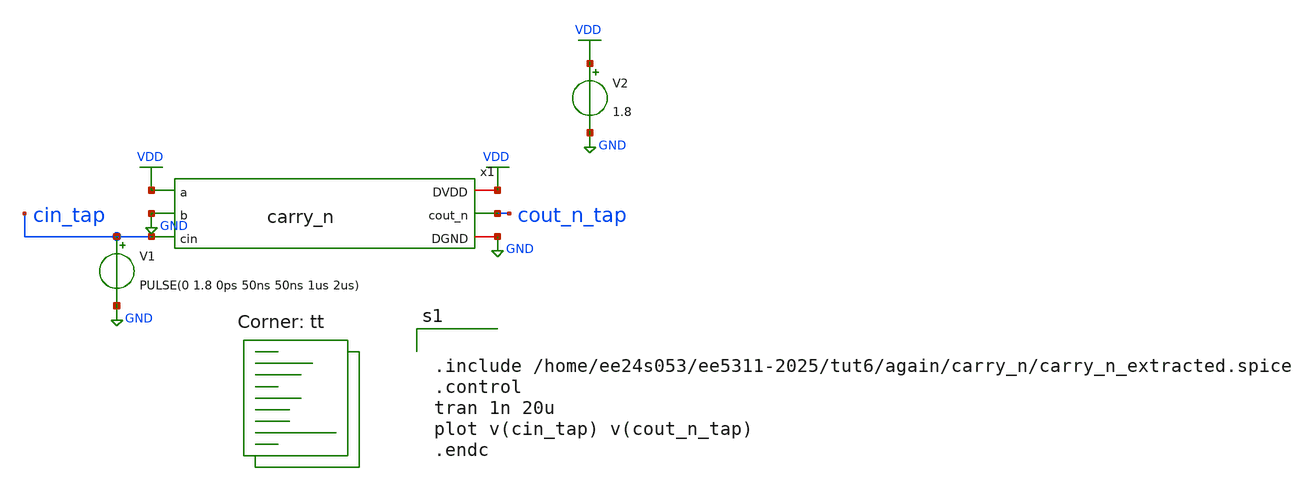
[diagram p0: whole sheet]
** sch_path: tut6/again/carry_n/carry_n_tb.sch
**.subckt carry_n_tb
x1 VDD VDD GND cout_n_tap cin_tap GND carry_n
V1 cin_tap GND PULSE(0 1.8 0ps 50ns 50ns 1us 2us)
V2 VDD GND 1.8
**** begin user architecture code
.lib $::SKYWATER_MODELS/sky130.lib.spice tt


.include /home/ee24s053/ee5311-2025/tut6/again/carry_n/carry_n_extracted.spice
.control
tran 1n 20u
plot v(cin_tap) v(cout_n_tap)
.endc


**** end user architecture code
**.ends
.GLOBAL VDD
.GLOBAL GND
.end
